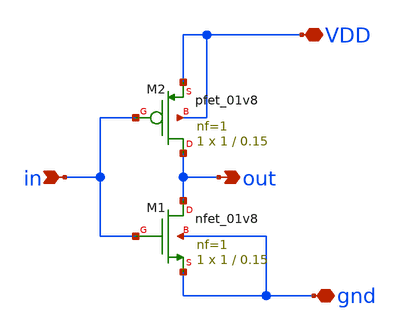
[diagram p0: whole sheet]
** sch_path: inverter/inverter.sch
**.subckt inverter in out VDD gnd
*.ipin in
*.opin out
*.iopin VDD
*.iopin gnd
XM1 out in gnd gnd sky130_fd_pr__nfet_01v8 L=0.15 W=1 nf=1 ad='int((nf+1)/2) * W/nf * 0.29' as='int((nf+2)/2) * W/nf * 0.29'
+ pd='2*int((nf+1)/2) * (W/nf + 0.29)' ps='2*int((nf+2)/2) * (W/nf + 0.29)' nrd='0.29 / W' nrs='0.29 / W'
+ sa=0 sb=0 sd=0 mult=1 m=1
XM2 out in VDD VDD sky130_fd_pr__pfet_01v8 L=0.15 W=1 nf=1 ad='int((nf+1)/2) * W/nf * 0.29' as='int((nf+2)/2) * W/nf * 0.29'
+ pd='2*int((nf+1)/2) * (W/nf + 0.29)' ps='2*int((nf+2)/2) * (W/nf + 0.29)' nrd='0.29 / W' nrs='0.29 / W'
+ sa=0 sb=0 sd=0 mult=1 m=1
**.ends
.end
